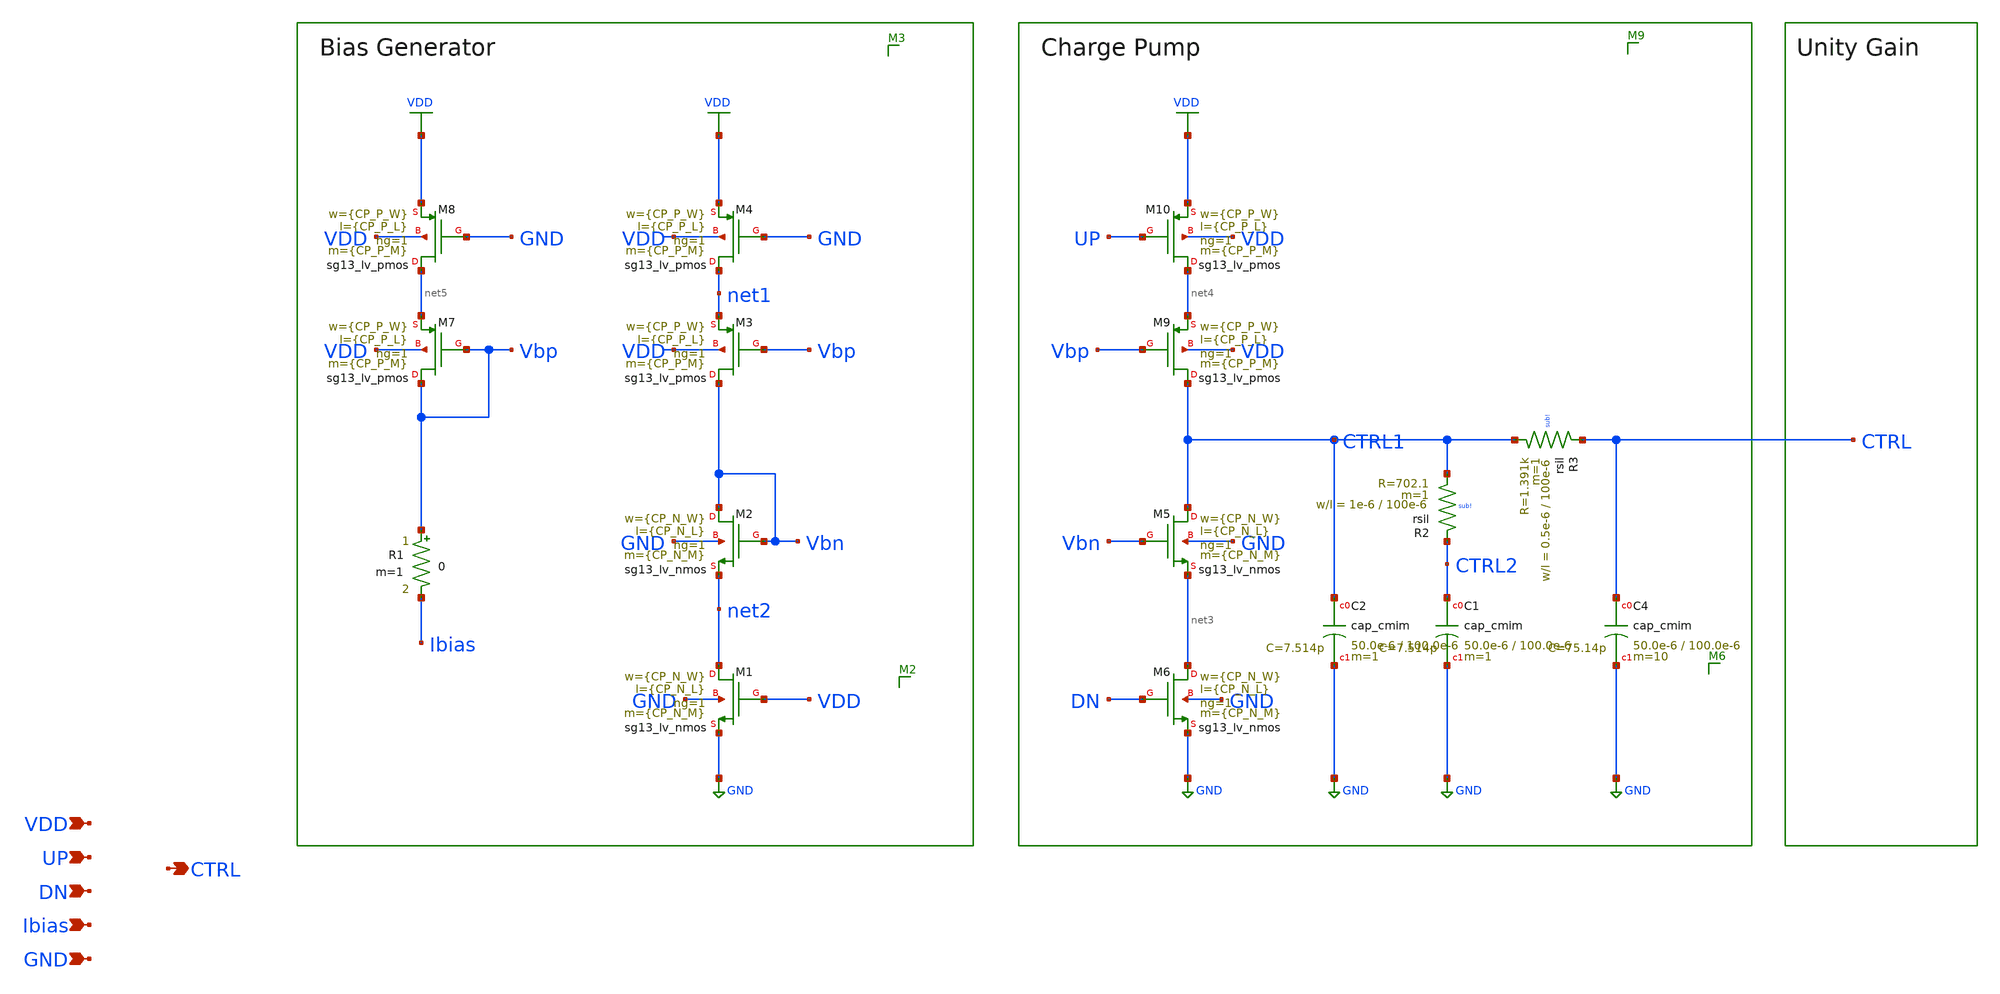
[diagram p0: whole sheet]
** sch_path: schematic/blocks/charge-pump/CP.sch
**.subckt CP CTRL UP VDD Ibias DN GND
*.opin CTRL
*.ipin UP
*.ipin VDD
*.ipin Ibias
*.ipin DN
*.ipin GND
XM2 Vbn Vbn net2 GND sg13_lv_nmos w={CP_N_W} l={CP_N_L} ng=1 m={CP_N_M} mm_ok=1
XM1 net2 VDD GND GND sg13_lv_nmos w={CP_N_W} l={CP_N_L} ng=1 m={CP_N_M} mm_ok=1
XM3 Vbn Vbp net1 VDD sg13_lv_pmos w={CP_P_W} l={CP_P_L} ng=1 m={CP_P_M} mm_ok=1
XM4 net1 GND VDD VDD sg13_lv_pmos w={CP_P_W} l={CP_P_L} ng=1 m={CP_P_M} mm_ok=1
XM7 Vbp Vbp net5 VDD sg13_lv_pmos w={CP_P_W} l={CP_P_L} ng=1 m={CP_P_M} mm_ok=1
XM8 net5 GND VDD VDD sg13_lv_pmos w={CP_P_W} l={CP_P_L} ng=1 m={CP_P_M} mm_ok=1
XM5 CTRL1 Vbn net3 GND sg13_lv_nmos w={CP_N_W} l={CP_N_L} ng=1 m={CP_N_M} mm_ok=1
XM6 net3 DN GND GND sg13_lv_nmos w={CP_N_W} l={CP_N_L} ng=1 m={CP_N_M} mm_ok=1
XM9 CTRL1 Vbp net4 VDD sg13_lv_pmos w={CP_P_W} l={CP_P_L} ng=1 m={CP_P_M} mm_ok=1
XM10 net4 UP VDD VDD sg13_lv_pmos w={CP_P_W} l={CP_P_L} ng=1 m={CP_P_M} mm_ok=1
XR3 CTRL CTRL1 sub! rsil w=0.5e-6 l=100e-6 m=1 mm_ok=1
XR2 CTRL2 CTRL1 sub! rsil w=1e-6 l=100e-6 m=1 mm_ok=1
R1 Vbp Ibias 0 m=1
XC4 CTRL GND cap_cmim w=50.0e-6 l=100.0e-6 m=10 mm_ok=1
XC1 CTRL2 GND cap_cmim w=50.0e-6 l=100.0e-6 m=1 mm_ok=1
XC2 CTRL1 GND cap_cmim w=50.0e-6 l=100.0e-6 m=1 mm_ok=1
**.ends
.GLOBAL GND
.GLOBAL VDD
.end
